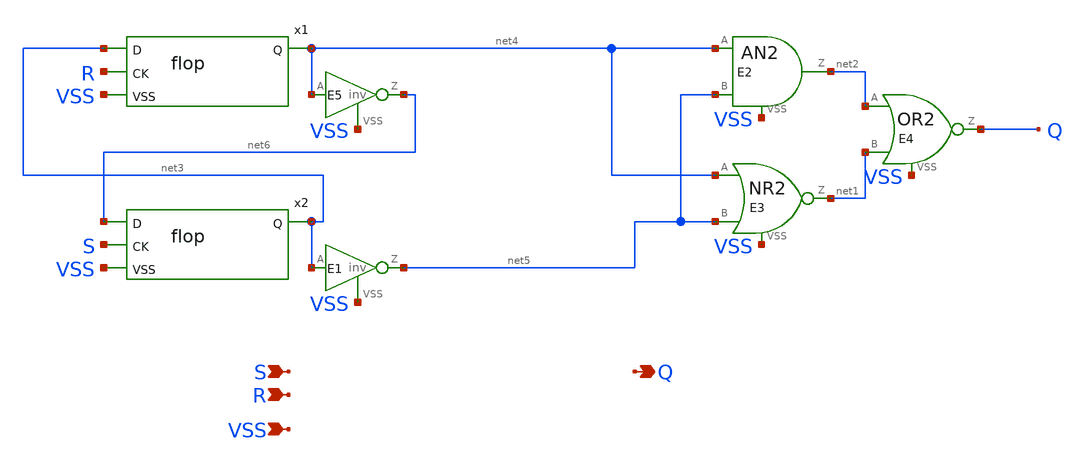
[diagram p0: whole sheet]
** sch_path: xschem_library/examples/sr_flop.sch
**.subckt sr_flop S Q VSS R
*.ipin S
*.opin Q
*.ipin VSS
*.ipin R
x1 net3 net4 R VSS flop VTH=VTH VHI=VHI
x2 net6 net3 S VSS flop VTH=VTH VHI=VHI
E2 net2 VSS and(2) net4 VSS net5 VSS 'VTH-0.1' 0.0 'VTH+0.1' VHI
E3 net1 VSS nor(2) net4 VSS net5 VSS 'VTH-0.1' VHI 'VTH+0.1' 0.0
E4 Q VSS or(2) net2 VSS net1 VSS 'VTH-0.1' 0.0 'VTH+0.1' VHI
E5 net6 VSS pwl(1) net4 VSS 'VTH-0.1' VHI 'VTH+0.1' 0
E1 net5 VSS pwl(1) net3 VSS 'VTH-0.1' VHI 'VTH+0.1' 0
**.ends
.end
